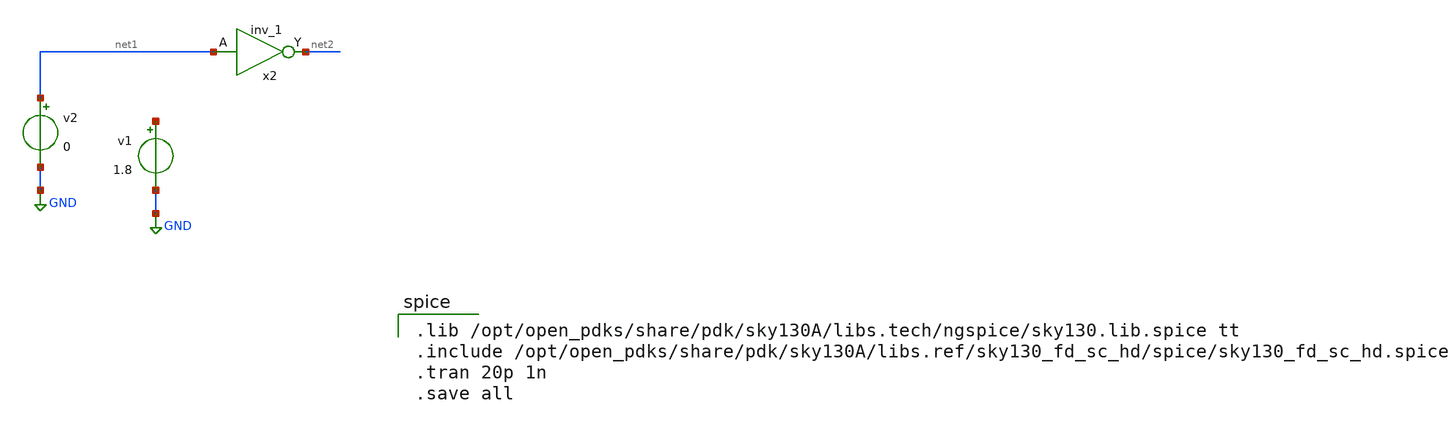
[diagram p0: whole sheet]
** sch_path: projects/carry_lookahead_adder/xschem/ports/test/true_table/std_inverter.sch
**.subckt std_inverter
v1 net3 GND 1.8
v2 net1 GND 0
x2 net1 GND GND net3 net3 net2 sky130_fd_sc_hd__inv_1
**** begin user architecture code

.lib /opt/open_pdks/share/pdk/sky130A/libs.tech/ngspice/sky130.lib.spice tt
.include /opt/open_pdks/share/pdk/sky130A/libs.ref/sky130_fd_sc_hd/spice/sky130_fd_sc_hd.spice
.tran 20p 1n
.save all

**** end user architecture code
**.ends
.GLOBAL GND
.end
